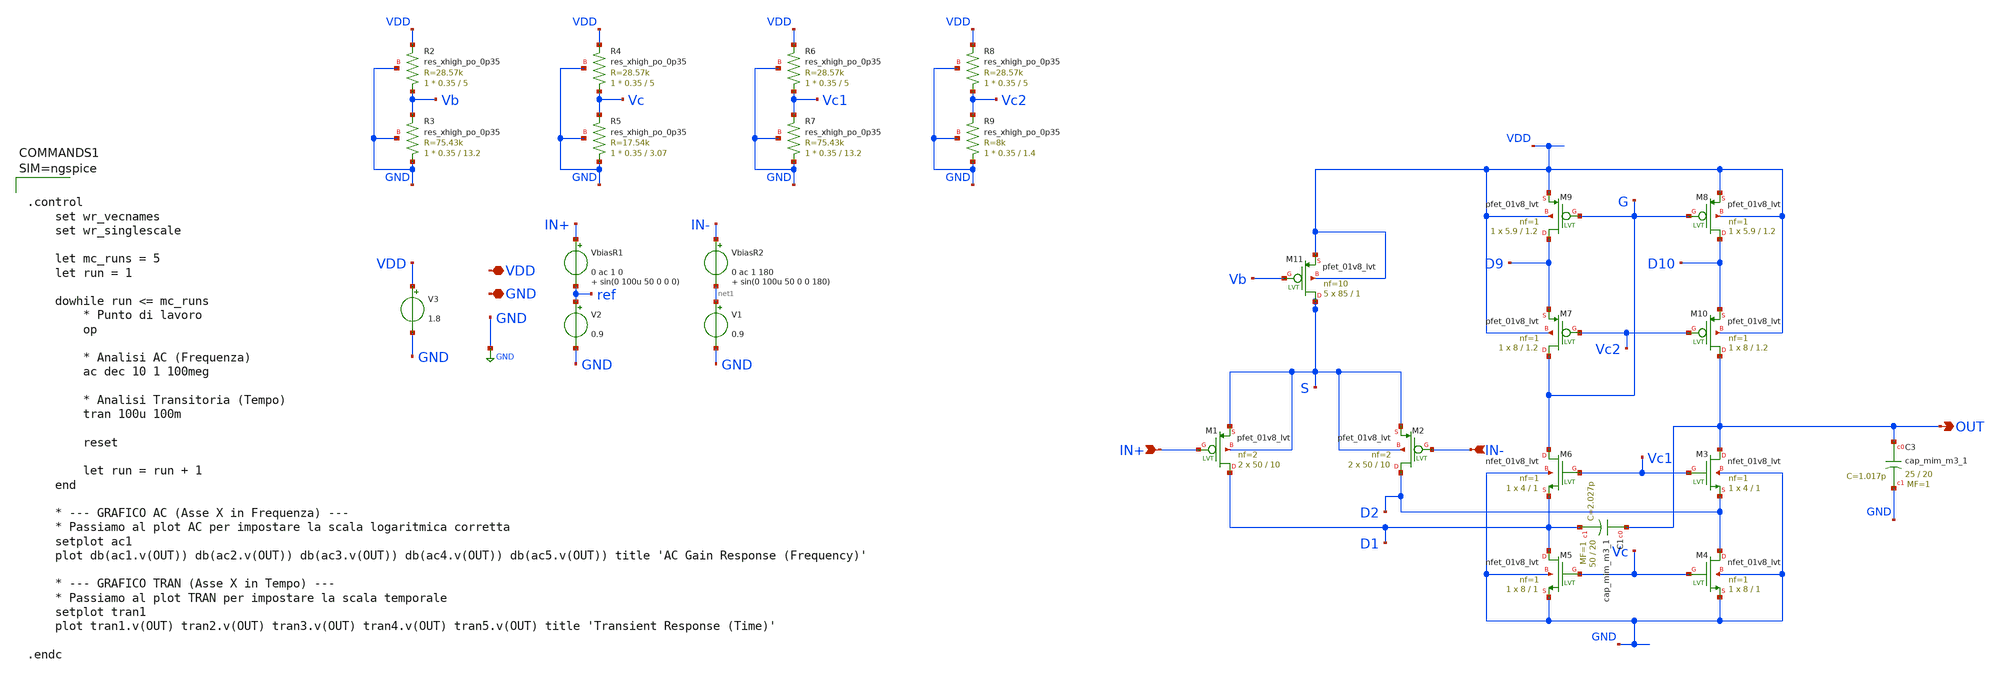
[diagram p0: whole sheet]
** sch_path: xschem/OTA_FoldedCascode_AC1_1_MC.sch
**.subckt OTA_FoldedCascode_AC1_1_MC OUT VDD GND IN+ IN-
*.opin OUT
*.iopin VDD
*.iopin GND
*.ipin IN+
*.ipin IN-
VbiasR1 IN+ ref 0 ac 1 0 sin(0 100u 50 0 0 0)
V2 ref GND 0.9
XC3 OUT GND sky130_fd_pr__cap_mim_m3_1 W=25 L=20 MF=1 m=1
V3 VDD GND 1.8
XM11 S Vb VDD VDD sky130_fd_pr__pfet_01v8_lvt L=1 W=85 nf=10 ad='int((nf+1)/2) * W/nf * 0.29' as='int((nf+2)/2) * W/nf * 0.29'
+ pd='2*int((nf+1)/2) * (W/nf + 0.29)' ps='2*int((nf+2)/2) * (W/nf + 0.29)' nrd='0.29 / W' nrs='0.29 / W'
+ sa=0 sb=0 sd=0 mult=5 m=5
XM1 D1 IN+ S S sky130_fd_pr__pfet_01v8_lvt L=10 W=50 nf=2 ad='int((nf+1)/2) * W/nf * 0.29' as='int((nf+2)/2) * W/nf * 0.29'
+ pd='2*int((nf+1)/2) * (W/nf + 0.29)' ps='2*int((nf+2)/2) * (W/nf + 0.29)' nrd='0.29 / W' nrs='0.29 / W'
+ sa=0 sb=0 sd=0 mult=2 m=2
XM2 D2 IN- S S sky130_fd_pr__pfet_01v8_lvt L=10 W=50 nf=2 ad='int((nf+1)/2) * W/nf * 0.29' as='int((nf+2)/2) * W/nf * 0.29'
+ pd='2*int((nf+1)/2) * (W/nf + 0.29)' ps='2*int((nf+2)/2) * (W/nf + 0.29)' nrd='0.29 / W' nrs='0.29 / W'
+ sa=0 sb=0 sd=0 mult=2 m=2
XM3 OUT Vc1 D2 GND sky130_fd_pr__nfet_01v8_lvt L=1 W=4 nf=1 ad='int((nf+1)/2) * W/nf * 0.29' as='int((nf+2)/2) * W/nf * 0.29'
+ pd='2*int((nf+1)/2) * (W/nf + 0.29)' ps='2*int((nf+2)/2) * (W/nf + 0.29)' nrd='0.29 / W' nrs='0.29 / W'
+ sa=0 sb=0 sd=0 mult=1 m=1
XM4 D2 Vc GND GND sky130_fd_pr__nfet_01v8_lvt L=1 W=8 nf=1 ad='int((nf+1)/2) * W/nf * 0.29' as='int((nf+2)/2) * W/nf * 0.29'
+ pd='2*int((nf+1)/2) * (W/nf + 0.29)' ps='2*int((nf+2)/2) * (W/nf + 0.29)' nrd='0.29 / W' nrs='0.29 / W'
+ sa=0 sb=0 sd=0 mult=1 m=1
XM5 D1 Vc GND GND sky130_fd_pr__nfet_01v8_lvt L=1 W=8 nf=1 ad='int((nf+1)/2) * W/nf * 0.29' as='int((nf+2)/2) * W/nf * 0.29'
+ pd='2*int((nf+1)/2) * (W/nf + 0.29)' ps='2*int((nf+2)/2) * (W/nf + 0.29)' nrd='0.29 / W' nrs='0.29 / W'
+ sa=0 sb=0 sd=0 mult=1 m=1
XM6 G Vc1 D1 GND sky130_fd_pr__nfet_01v8_lvt L=1 W=4 nf=1 ad='int((nf+1)/2) * W/nf * 0.29' as='int((nf+2)/2) * W/nf * 0.29'
+ pd='2*int((nf+1)/2) * (W/nf + 0.29)' ps='2*int((nf+2)/2) * (W/nf + 0.29)' nrd='0.29 / W' nrs='0.29 / W'
+ sa=0 sb=0 sd=0 mult=1 m=1
XR2 Vb VDD GND sky130_fd_pr__res_xhigh_po_0p35 L=5 mult=1 m=1
XR3 GND Vb GND sky130_fd_pr__res_xhigh_po_0p35 L=13.2 mult=1 m=1
XR4 Vc VDD GND sky130_fd_pr__res_xhigh_po_0p35 L=5 mult=1 m=1
XR5 GND Vc GND sky130_fd_pr__res_xhigh_po_0p35 L=3.07 mult=1 m=1
XR6 Vc1 VDD GND sky130_fd_pr__res_xhigh_po_0p35 L=5 mult=1 m=1
XR7 GND Vc1 GND sky130_fd_pr__res_xhigh_po_0p35 L=13.2 mult=1 m=1
XR8 Vc2 VDD GND sky130_fd_pr__res_xhigh_po_0p35 L=5 mult=1 m=1
XR9 GND Vc2 GND sky130_fd_pr__res_xhigh_po_0p35 L=1.4 mult=1 m=1
XM7 G Vc2 D9 VDD sky130_fd_pr__pfet_01v8_lvt L=1.2 W=8 nf=1 ad='int((nf+1)/2) * W/nf * 0.29' as='int((nf+2)/2) * W/nf * 0.29'
+ pd='2*int((nf+1)/2) * (W/nf + 0.29)' ps='2*int((nf+2)/2) * (W/nf + 0.29)' nrd='0.29 / W' nrs='0.29 / W'
+ sa=0 sb=0 sd=0 mult=1 m=1
XM9 D9 G VDD VDD sky130_fd_pr__pfet_01v8_lvt L=1.2 W=5.9 nf=1 ad='int((nf+1)/2) * W/nf * 0.29' as='int((nf+2)/2) * W/nf * 0.29'
+ pd='2*int((nf+1)/2) * (W/nf + 0.29)' ps='2*int((nf+2)/2) * (W/nf + 0.29)' nrd='0.29 / W' nrs='0.29 / W'
+ sa=0 sb=0 sd=0 mult=1 m=1
XM8 D10 G VDD VDD sky130_fd_pr__pfet_01v8_lvt L=1.2 W=5.9 nf=1 ad='int((nf+1)/2) * W/nf * 0.29' as='int((nf+2)/2) * W/nf * 0.29'
+ pd='2*int((nf+1)/2) * (W/nf + 0.29)' ps='2*int((nf+2)/2) * (W/nf + 0.29)' nrd='0.29 / W' nrs='0.29 / W'
+ sa=0 sb=0 sd=0 mult=1 m=1
XM10 OUT Vc2 D10 VDD sky130_fd_pr__pfet_01v8_lvt L=1.2 W=8 nf=1 ad='int((nf+1)/2) * W/nf * 0.29' as='int((nf+2)/2) * W/nf * 0.29'
+ pd='2*int((nf+1)/2) * (W/nf + 0.29)' ps='2*int((nf+2)/2) * (W/nf + 0.29)' nrd='0.29 / W' nrs='0.29 / W'
+ sa=0 sb=0 sd=0 mult=1 m=1
XC1 OUT D1 sky130_fd_pr__cap_mim_m3_1 W=50 L=20 MF=1 m=1
VbiasR2 IN- net1 0 ac 1 180 sin(0 100u 50 0 0 180)
V1 net1 GND 0.9
**** begin user architecture code



.control
    set wr_vecnames
    set wr_singlescale

    let mc_runs = 5
    let run = 1

    dowhile run <= mc_runs
        * Punto di lavoro
        op

        * Analisi AC (Frequenza)
        ac dec 10 1 100meg

        * Analisi Transitoria (Tempo)
        tran 100u 100m

        reset

        let run = run + 1
    end

    * --- GRAFICO AC (Asse X in Frequenza) ---
    * Passiamo al plot AC per impostare la scala logaritmica corretta
    setplot ac1
    plot db(ac1.v(OUT)) db(ac2.v(OUT)) db(ac3.v(OUT)) db(ac4.v(OUT)) db(ac5.v(OUT)) title 'AC Gain Response (Frequency)'

    * --- GRAFICO TRAN (Asse X in Tempo) ---
    * Passiamo al plot TRAN per impostare la scala temporale
    setplot tran1
    plot tran1.v(OUT) tran2.v(OUT) tran3.v(OUT) tran4.v(OUT) tran5.v(OUT) title 'Transient Response (Time)'

.endc



.lib $::SKYWATER_MODELS/sky130.lib.spice tt_mm
**** end user architecture code
**.ends
.GLOBAL GND
.end
